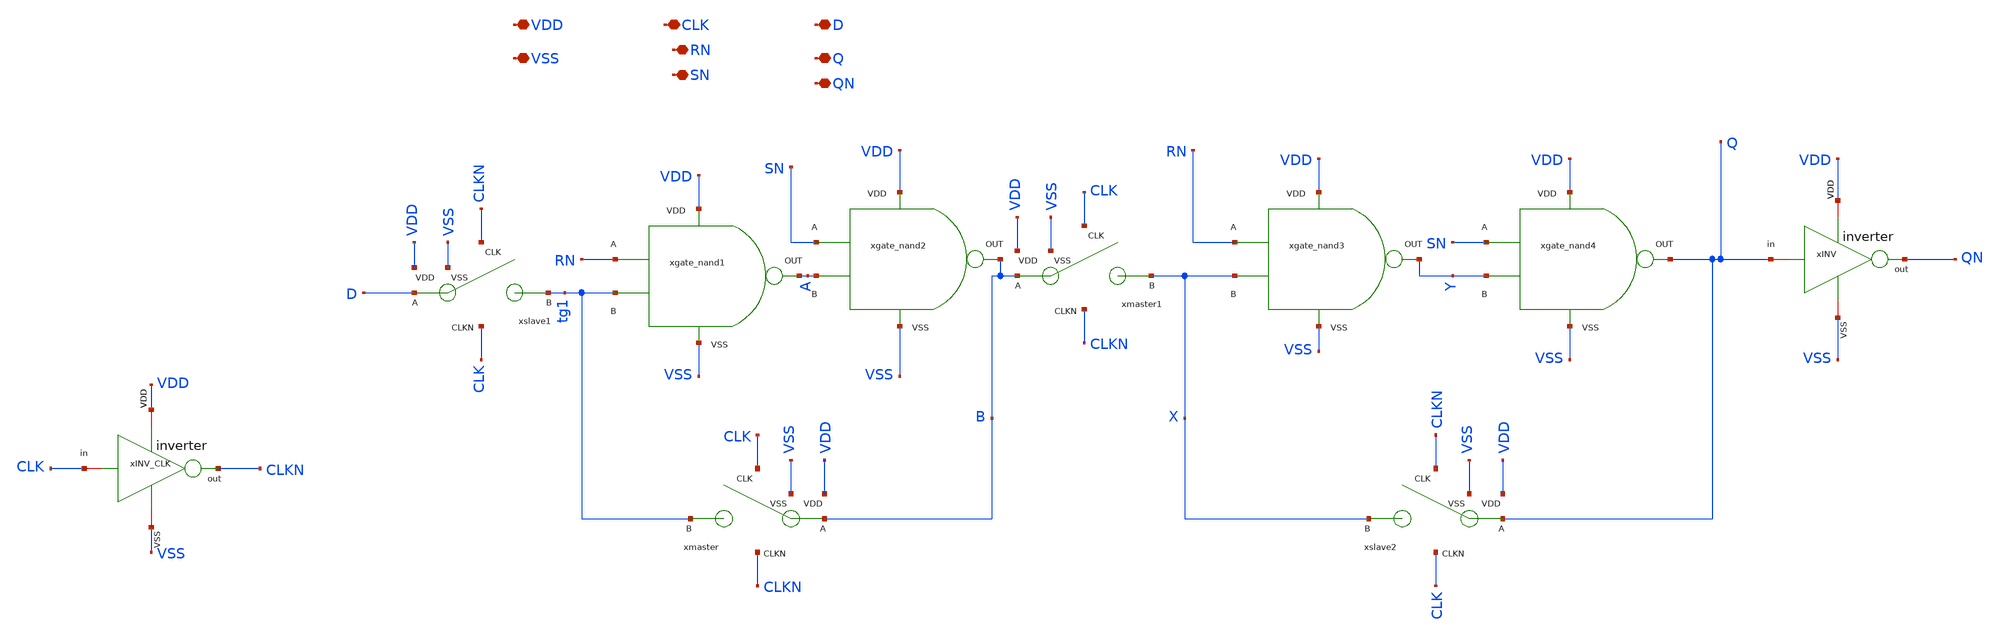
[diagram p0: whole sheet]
** sch_path: designs/sar_adc/digital/flip_flop_set/xschem/flip_flop_set.sch
**.subckt flip_flop_set VDD VSS CLK D RN Q QN SN
*.iopin VDD
*.iopin VSS
*.iopin CLK
*.iopin D
*.iopin RN
*.iopin Q
*.iopin QN
*.iopin SN
xslave1 CLKN D VDD tg1 CLK VSS TG
xslave2 CLKN Q VDD X CLK VSS TG
xmaster CLK B VDD tg1 CLKN VSS TG
xgate_nand1 VDD VSS RN tg1 A NAND
xINV_CLK VDD CLK CLKN VSS inverter
xINV VDD Q QN VSS inverter
xmaster1 CLK B VDD X CLKN VSS TG
xgate_nand2 VDD VSS SN A B NAND
xgate_nand3 VDD VSS RN X Y NAND
xgate_nand4 VDD VSS SN Y Q NAND
**.ends

* expanding   symbol:  designs/sar_adc/digital/TG/xschem/TG.sym # of pins=6
** sym_path: designs/sar_adc/digital/TG/xschem/TG.sym
** sch_path: designs/sar_adc/digital/TG/xschem/TG.sch
.subckt TG CLK A VDD B CLKN VSS
*.iopin VDD
*.iopin VSS
*.ipin CLK
*.ipin CLKN
*.iopin A
*.iopin B
XM1 A CLK B VSS nfet_03v3 L=0.28u W=0.22u nf=1 ad='int((nf+1)/2) * W/nf * 0.18u' as='int((nf+2)/2) * W/nf * 0.18u'
+ pd='2*int((nf+1)/2) * (W/nf + 0.18u)' ps='2*int((nf+2)/2) * (W/nf + 0.18u)' nrd='0.18u / W' nrs='0.18u / W'
+ sa=0 sb=0 sd=0 m=1
XM2 A CLKN B VDD pfet_03v3 L=0.28u W=0.22u nf=1 ad='int((nf+1)/2) * W/nf * 0.18u' as='int((nf+2)/2) * W/nf * 0.18u'
+ pd='2*int((nf+1)/2) * (W/nf + 0.18u)' ps='2*int((nf+2)/2) * (W/nf + 0.18u)' nrd='0.18u / W' nrs='0.18u / W'
+ sa=0 sb=0 sd=0 m=1
.ends


* expanding   symbol:  designs/sar_adc/digital/NAND/xschem/NAND.sym # of pins=5
** sym_path: designs/sar_adc/digital/NAND/xschem/NAND.sym
** sch_path: designs/sar_adc/digital/NAND/xschem/NAND.sch
.subckt NAND VDD VSS A B out
*.iopin A
*.iopin B
*.iopin out
*.iopin VDD
*.iopin VSS
xINVA1 VDD net1 net2 VSS inverter
xINVB1 VDD net2 out VSS inverter
XM5 net1 A VDD VDD pfet_03v3 L=0.28u W=0.5u nf=1 ad='int((nf+1)/2) * W/nf * 0.18u' as='int((nf+2)/2) * W/nf * 0.18u'
+ pd='2*int((nf+1)/2) * (W/nf + 0.18u)' ps='2*int((nf+2)/2) * (W/nf + 0.18u)' nrd='0.18u / W' nrs='0.18u / W'
+ sa=0 sb=0 sd=0 m=2
XM6 net1 A net3 VSS nfet_03v3 L=0.28u W=0.5u nf=1 ad='int((nf+1)/2) * W/nf * 0.18u' as='int((nf+2)/2) * W/nf * 0.18u'
+ pd='2*int((nf+1)/2) * (W/nf + 0.18u)' ps='2*int((nf+2)/2) * (W/nf + 0.18u)' nrd='0.18u / W' nrs='0.18u / W'
+ sa=0 sb=0 sd=0 m=1
XM7 net1 B VDD VDD pfet_03v3 L=0.28u W=0.5u nf=1 ad='int((nf+1)/2) * W/nf * 0.18u' as='int((nf+2)/2) * W/nf * 0.18u'
+ pd='2*int((nf+1)/2) * (W/nf + 0.18u)' ps='2*int((nf+2)/2) * (W/nf + 0.18u)' nrd='0.18u / W' nrs='0.18u / W'
+ sa=0 sb=0 sd=0 m=2
XM8 net3 B VSS VSS nfet_03v3 L=0.28u W=0.5u nf=1 ad='int((nf+1)/2) * W/nf * 0.18u' as='int((nf+2)/2) * W/nf * 0.18u'
+ pd='2*int((nf+1)/2) * (W/nf + 0.18u)' ps='2*int((nf+2)/2) * (W/nf + 0.18u)' nrd='0.18u / W' nrs='0.18u / W'
+ sa=0 sb=0 sd=0 m=1
.ends


* expanding   symbol:  designs/sar_adc/digital/inverter/xschem/inverter.sym # of pins=6
** sym_path: designs/sar_adc/digital/inverter/xschem/inverter.sym
** sch_path: designs/sar_adc/digital/inverter/xschem/inverter.sch
.subckt inverter VDD in out VSS
*.opin out
*.iopin in
*.iopin VDD
*.iopin VSS
XM1 out in VSS VSS nfet_03v3 L=0.28u W=1u nf=1 ad='int((nf+1)/2) * W/nf * 0.18u' as='int((nf+2)/2) * W/nf * 0.18u'
+ pd='2*int((nf+1)/2) * (W/nf + 0.18u)' ps='2*int((nf+2)/2) * (W/nf + 0.18u)' nrd='0.18u / W' nrs='0.18u / W'
+ sa=0 sb=0 sd=0 m=1
XM2 out in VDD VDD pfet_03v3 L=0.28u W=3u nf=1 ad='int((nf+1)/2) * W/nf * 0.18u' as='int((nf+2)/2) * W/nf * 0.18u'
+ pd='2*int((nf+1)/2) * (W/nf + 0.18u)' ps='2*int((nf+2)/2) * (W/nf + 0.18u)' nrd='0.18u / W' nrs='0.18u / W'
+ sa=0 sb=0 sd=0 m=1
.ends

.end
